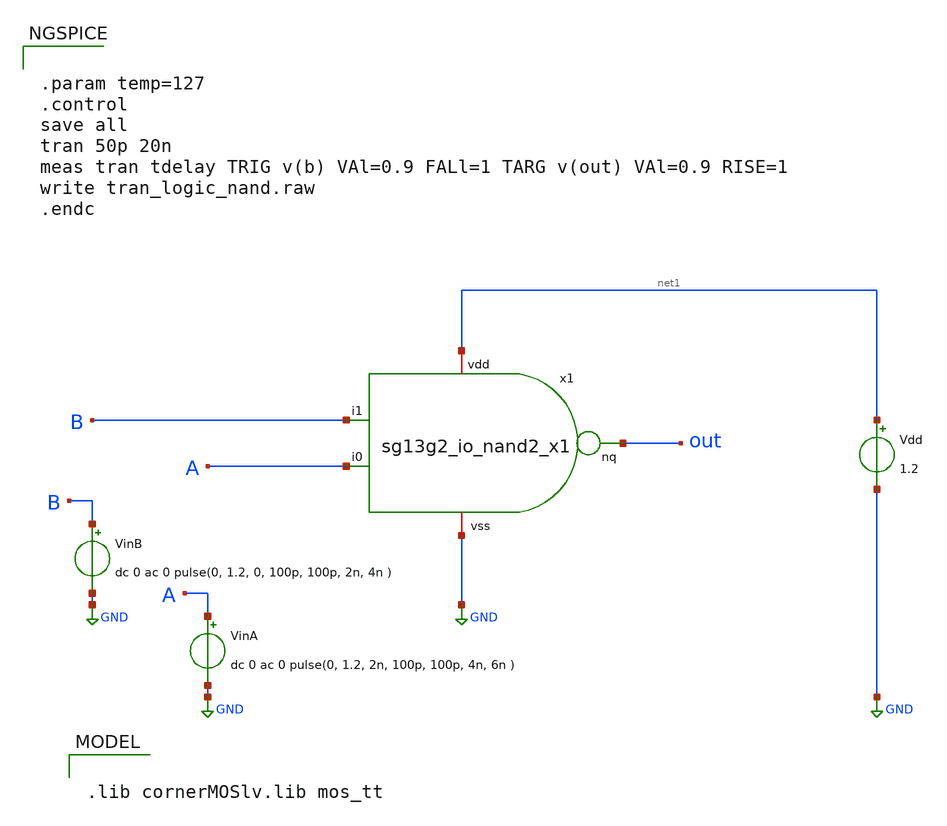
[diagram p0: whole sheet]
** sch_path: ihp-sg13g2/libs.ref/sg13g2_io/xschem/io_testbench/sg13g2_io_nand2_x1_tb.sch
* Copyright 2023 IHP PDK Authors
**.subckt sg13g2_io_nand2_x1_tb
VinA A GND dc 0 ac 0 pulse(0, 1.2, 2n, 100p, 100p, 4n, 6n )
Vdd net1 GND 1.2
VinB B GND dc 0 ac 0 pulse(0, 1.2, 0, 100p, 100p, 2n, 4n )
x1 net1 out B A GND sg13g2_io_nand2_x1
**** begin user architecture code

.lib cornerMOSlv.lib mos_tt



.param temp=127
.control
save all
tran 50p 20n
meas tran tdelay TRIG v(b) VAl=0.9 FALl=1 TARG v(out) VAl=0.9 RISE=1
write tran_logic_nand.raw
.endc


**** end user architecture code
**.ends

* expanding   symbol:  sg13g2_io_nand2_x1.sym # of pins=5
** sym_path: ihp-sg13g2/libs.ref/sg13g2_io/xschem/sg13g2_io_nand2_x1.sym
** sch_path: ihp-sg13g2/libs.ref/sg13g2_io/xschem/sg13g2_io_nand2_x1.sch
.subckt sg13g2_io_nand2_x1 vdd nq i1 i0 vss
*.iopin vdd
*.iopin vss
*.ipin i0
*.ipin i1
*.opin nq
XM1 net1 i1 nq vss sg13_lv_nmos w=3.93u l=0.13u ng=1 m=1 mm_ok=1
XM2 nq i1 vdd vdd sg13_lv_pmos w=4.41u l=0.13u ng=1 m=1 mm_ok=1
XM3 net1 i1 nq vss sg13_lv_nmos w=3.93u l=0.13u ng=1 m=1 mm_ok=1
XM4 vss i0 net1 vss sg13_lv_nmos w=3.93u l=0.13u ng=1 m=1 mm_ok=1
XM5 nq i0 vdd vdd sg13_lv_pmos w=4.41u l=0.13u ng=1 m=1 mm_ok=1
.ends

.GLOBAL GND
.end
